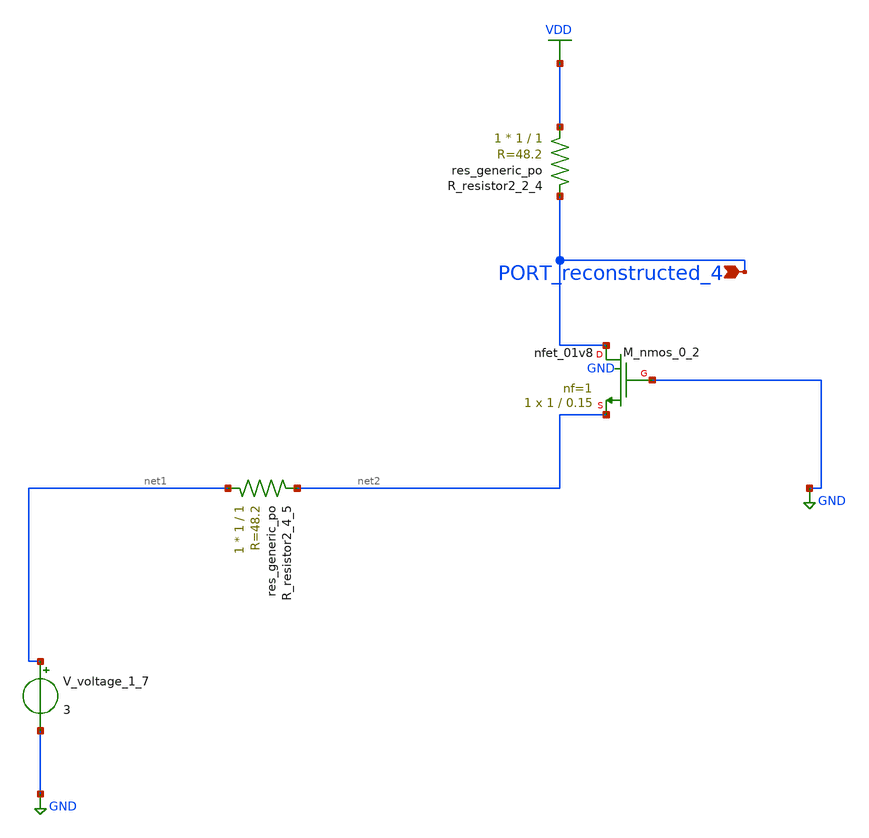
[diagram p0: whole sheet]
** sch_path: schematics/AMSNet/200.sch
**.subckt 200 PORT_reconstructed_4
*.ipin PORT_reconstructed_4
XM_nmos_0_2 PORT_reconstructed_4 GND net2 GND sky130_fd_pr__nfet_01v8 L=0.15 W=1 nf=1 ad='int((1 + 1)/2) * 1 / 1 * 0.29'
+ as='int((1 + 2)/2) * 1 / 1 * 0.29' pd='2*int((1 + 1)/2) * (1 / 1 + 0.29)' ps='2*int((1 + 2)/2) * (1 / 1 + 0.29)'
+ nrd='0.29 / 1 ' nrs='0.29 / 1 ' sa=0 sb=0 sd=0 mult=1 m=1
XR_resistor2_2_4 VDD PORT_reconstructed_4 sky130_fd_pr__res_generic_po W=1 L=1 m=1
XR_resistor2_4_5 net1 net2 sky130_fd_pr__res_generic_po W=1 L=1 m=1
V_voltage_1_7 net1 GND 3
**.ends
.GLOBAL GND
.GLOBAL VDD
.end
